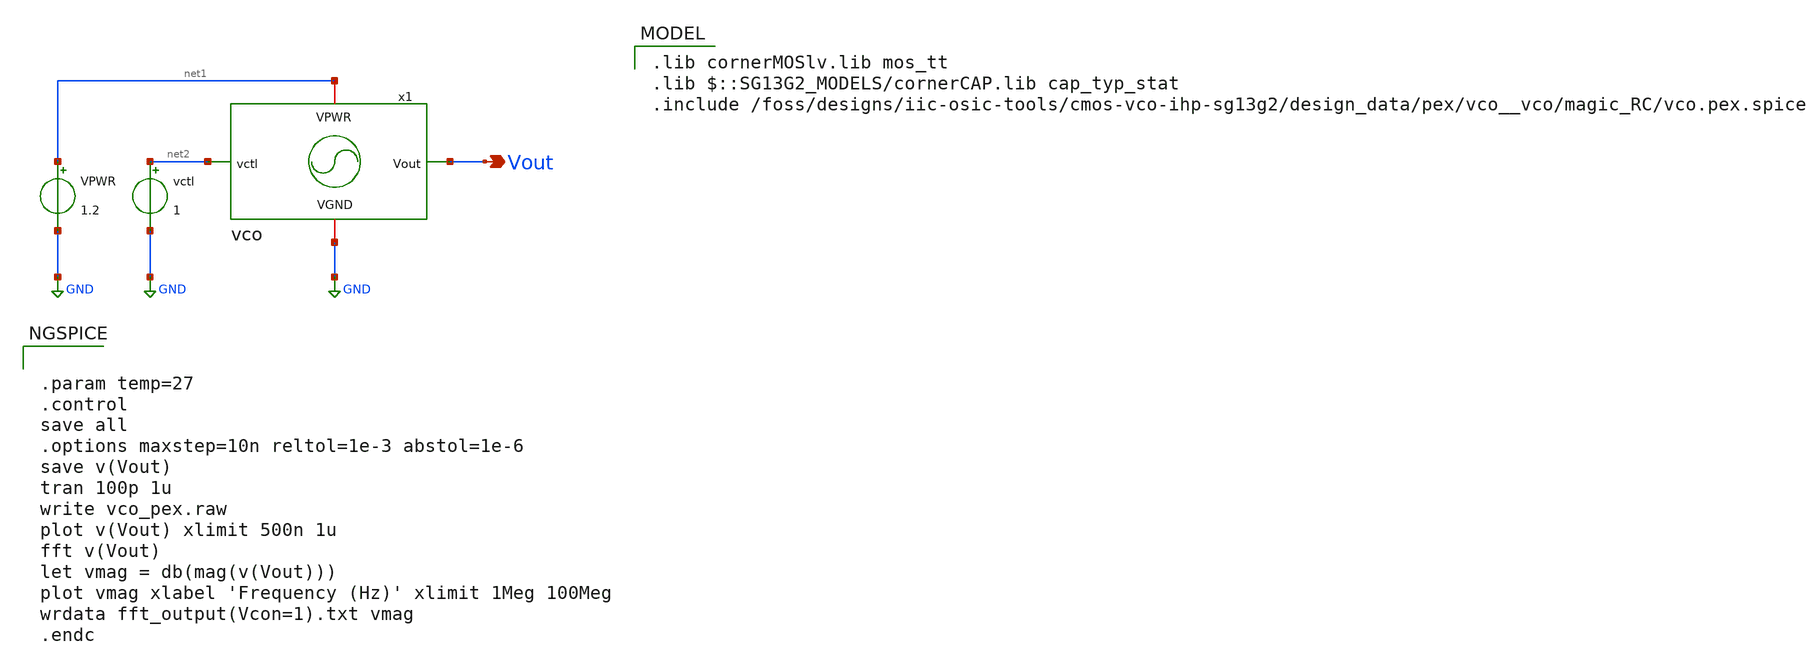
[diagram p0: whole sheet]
** sch_path: design_data/xschem/vco_pex_tb.sch
**.subckt vco_pex_tb Vout
*.opin Vout
VPWR net1 GND 1.2
vctl net2 GND 1
x1 net1 GND net2 Vout vco
**** begin user architecture code
 .lib cornerMOSlv.lib mos_tt
.lib $::SG13G2_MODELS/cornerCAP.lib cap_typ_stat
.include /foss/designs/iic-osic-tools/cmos-vco-ihp-sg13g2/design_data/pex/vco__vco/magic_RC/vco.pex.spice




.param temp=27
.control
save all
.options maxstep=10n reltol=1e-3 abstol=1e-6
save v(Vout)
tran 100p 1u
write vco_pex.raw
plot v(Vout) xlimit 500n 1u
fft v(Vout)
let vmag = db(mag(v(Vout)))
plot vmag xlabel 'Frequency (Hz)' xlimit 1Meg 100Meg
wrdata fft_output(Vcon=1).txt vmag
.endc


**** end user architecture code
**.ends
.GLOBAL GND
.end
